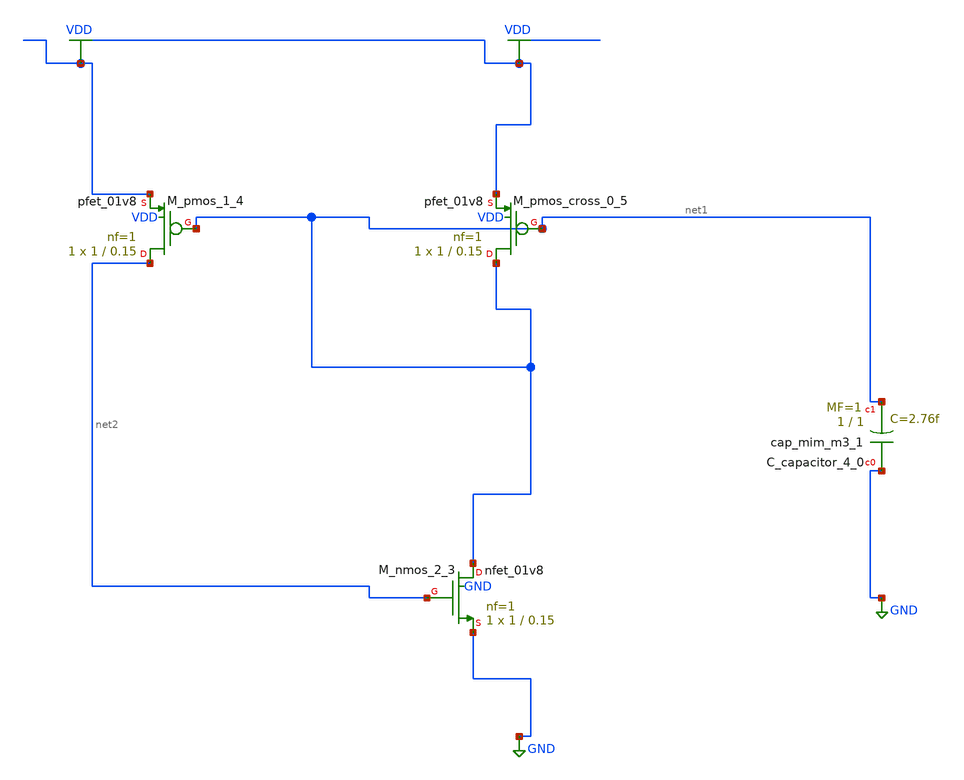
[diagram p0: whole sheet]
** sch_path: schematics/AMSNet/345.sch
**.subckt 345
XC_capacitor_4_0 GND net1 sky130_fd_pr__cap_mim_m3_1 W=1 L=1 MF=1 m=1
XM_nmos_2_3 net1 net2 GND GND sky130_fd_pr__nfet_01v8 L=0.15 W=1 nf=1 ad='int((1 + 1)/2) * 1 / 1 * 0.29'
+ as='int((1 + 2)/2) * 1 / 1 * 0.29' pd='2*int((1 + 1)/2) * (1 / 1 + 0.29)' ps='2*int((1 + 2)/2) * (1 / 1 + 0.29)'
+ nrd='0.29 / 1 ' nrs='0.29 / 1 ' sa=0 sb=0 sd=0 mult=1 m=1
XM_pmos_1_4 net2 net1 VDD VDD sky130_fd_pr__pfet_01v8 L=0.15 W=1 nf=1 ad='int((1 + 1)/2) * 1 / 1 * 0.29'
+ as='int((1 + 2)/2) * 1 / 1 * 0.29' pd='2*int((1 + 1)/2) * (1 / 1 + 0.29)' ps='2*int((1 + 2)/2) * (1 / 1 + 0.29)'
+ nrd='0.29 / 1 ' nrs='0.29 / 1 ' sa=0 sb=0 sd=0 mult=1 m=1
XM_pmos_cross_0_5 net1 net1 VDD VDD sky130_fd_pr__pfet_01v8 L=0.15 W=1 nf=1 ad='int((1 + 1)/2) * 1 / 1 * 0.29'
+ as='int((1 + 2)/2) * 1 / 1 * 0.29' pd='2*int((1 + 1)/2) * (1 / 1 + 0.29)' ps='2*int((1 + 2)/2) * (1 / 1 + 0.29)'
+ nrd='0.29 / 1 ' nrs='0.29 / 1 ' sa=0 sb=0 sd=0 mult=1 m=1
**.ends
.GLOBAL GND
.GLOBAL VDD
.end
